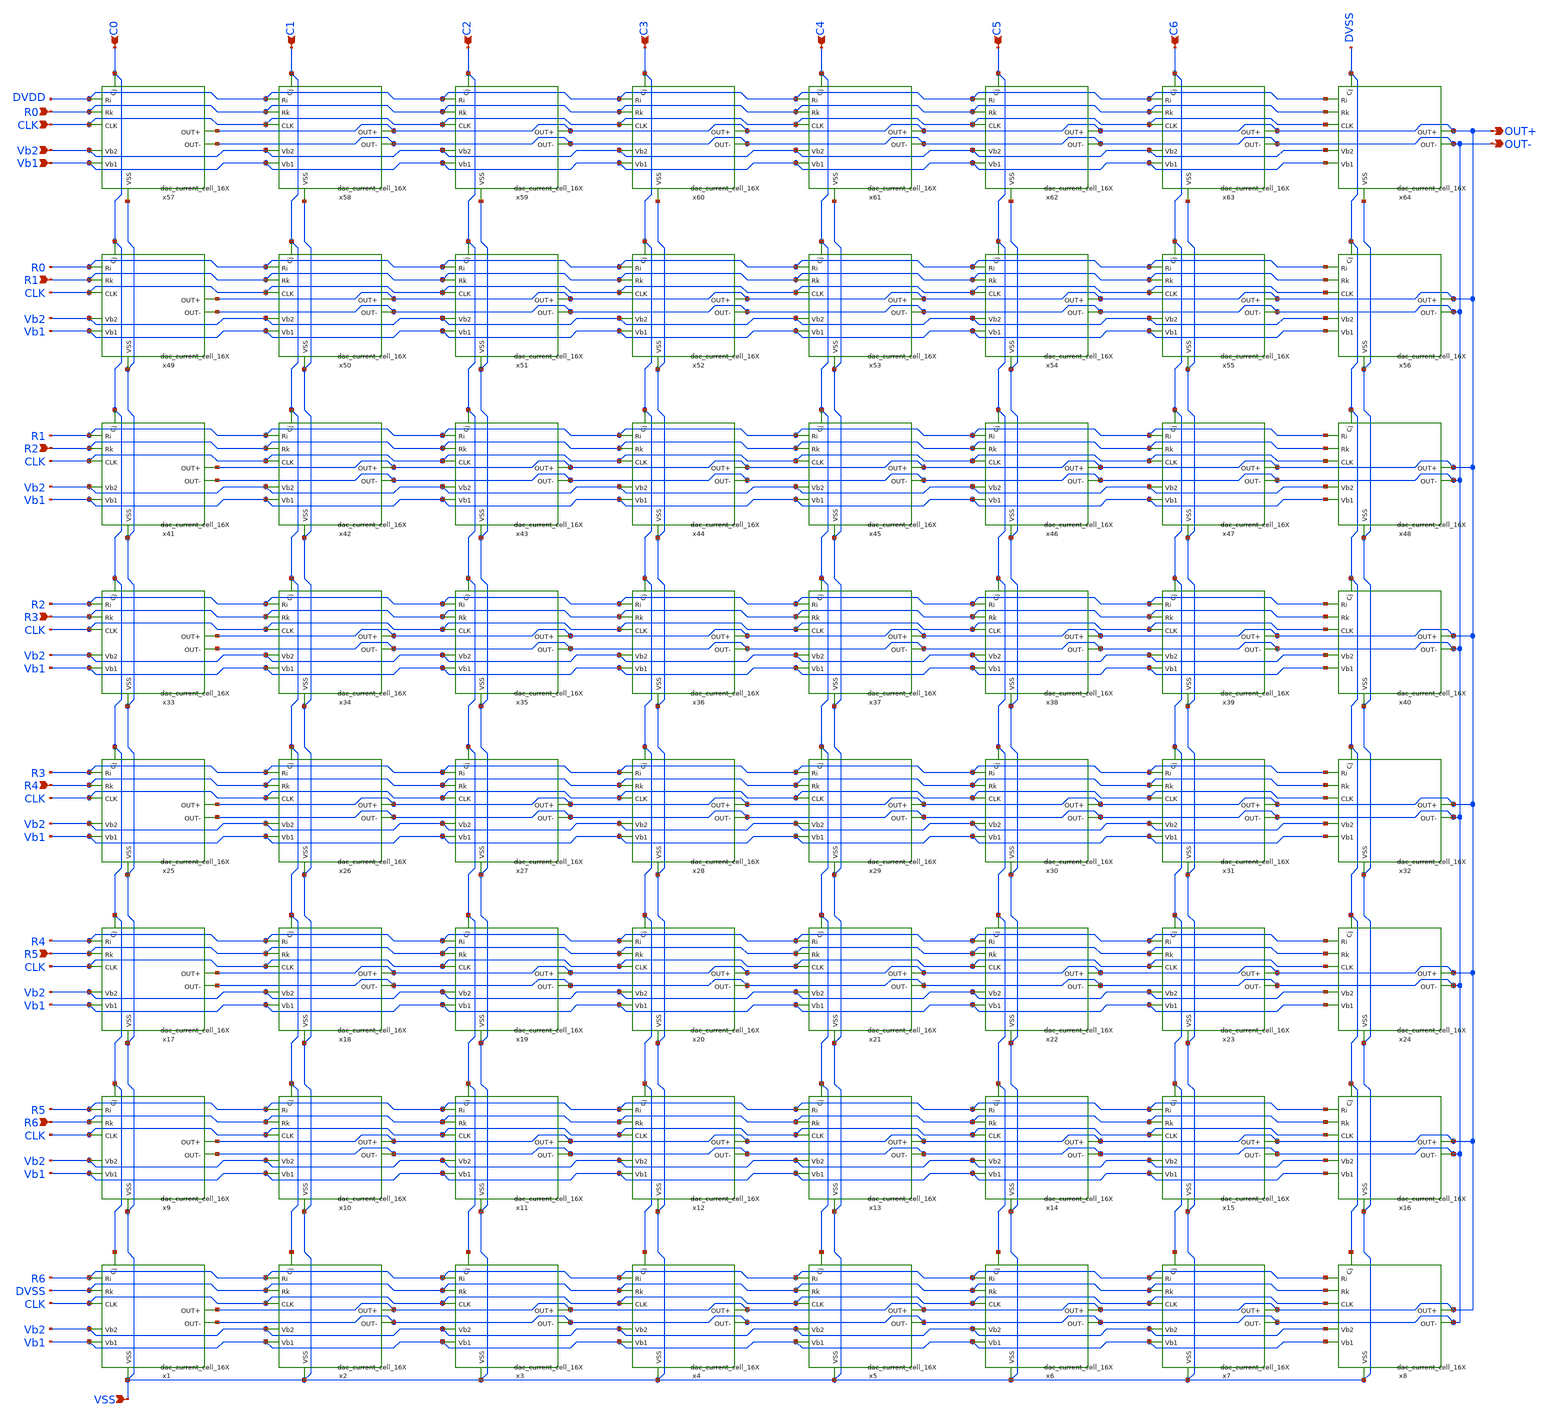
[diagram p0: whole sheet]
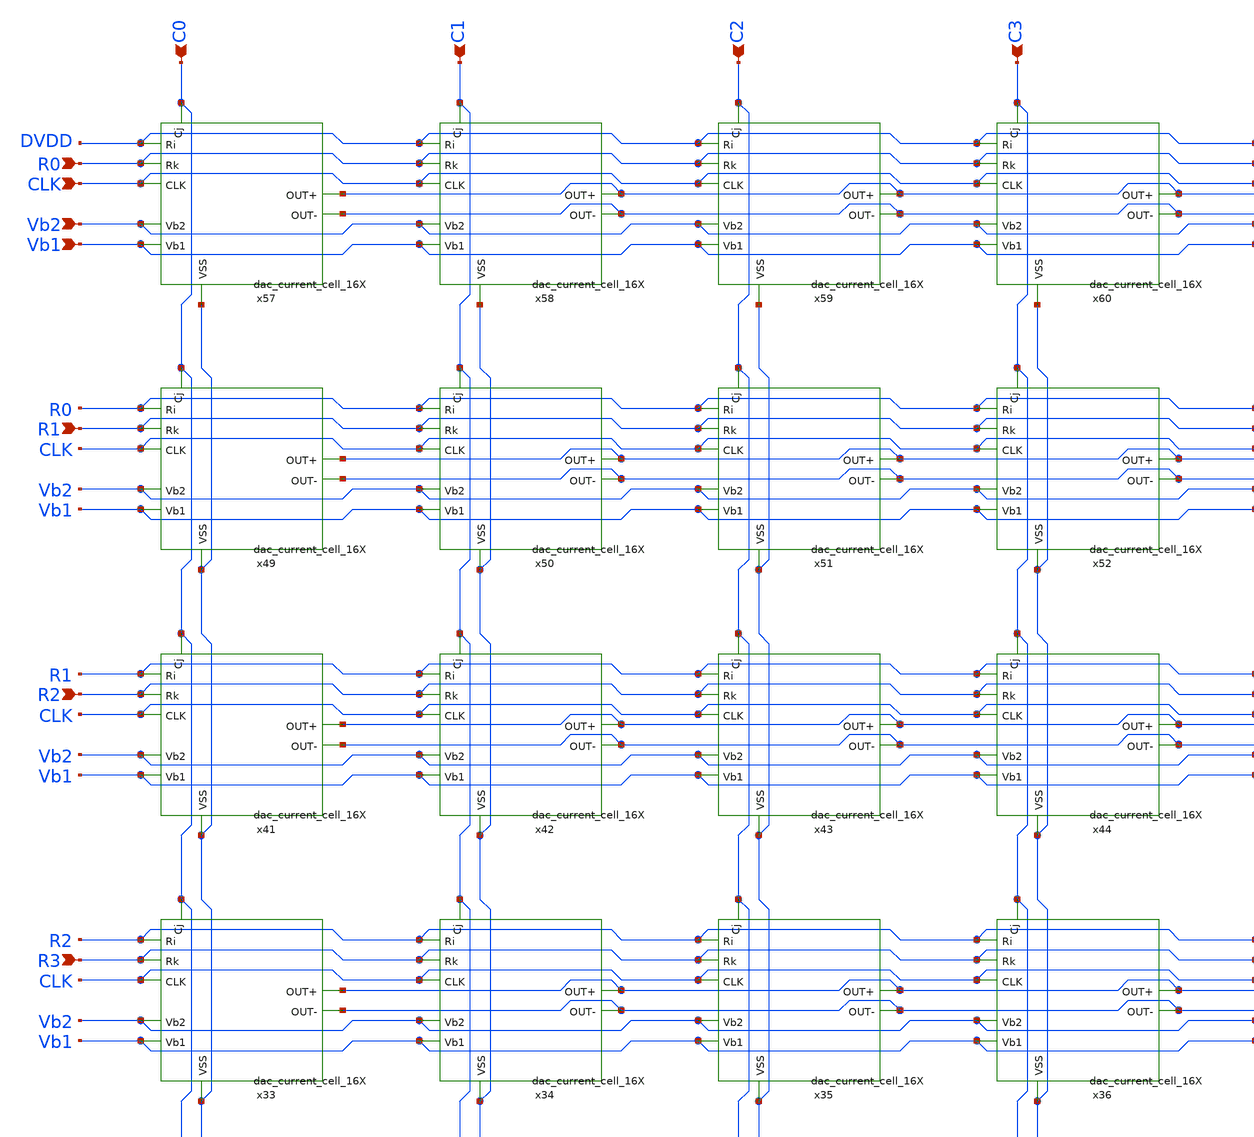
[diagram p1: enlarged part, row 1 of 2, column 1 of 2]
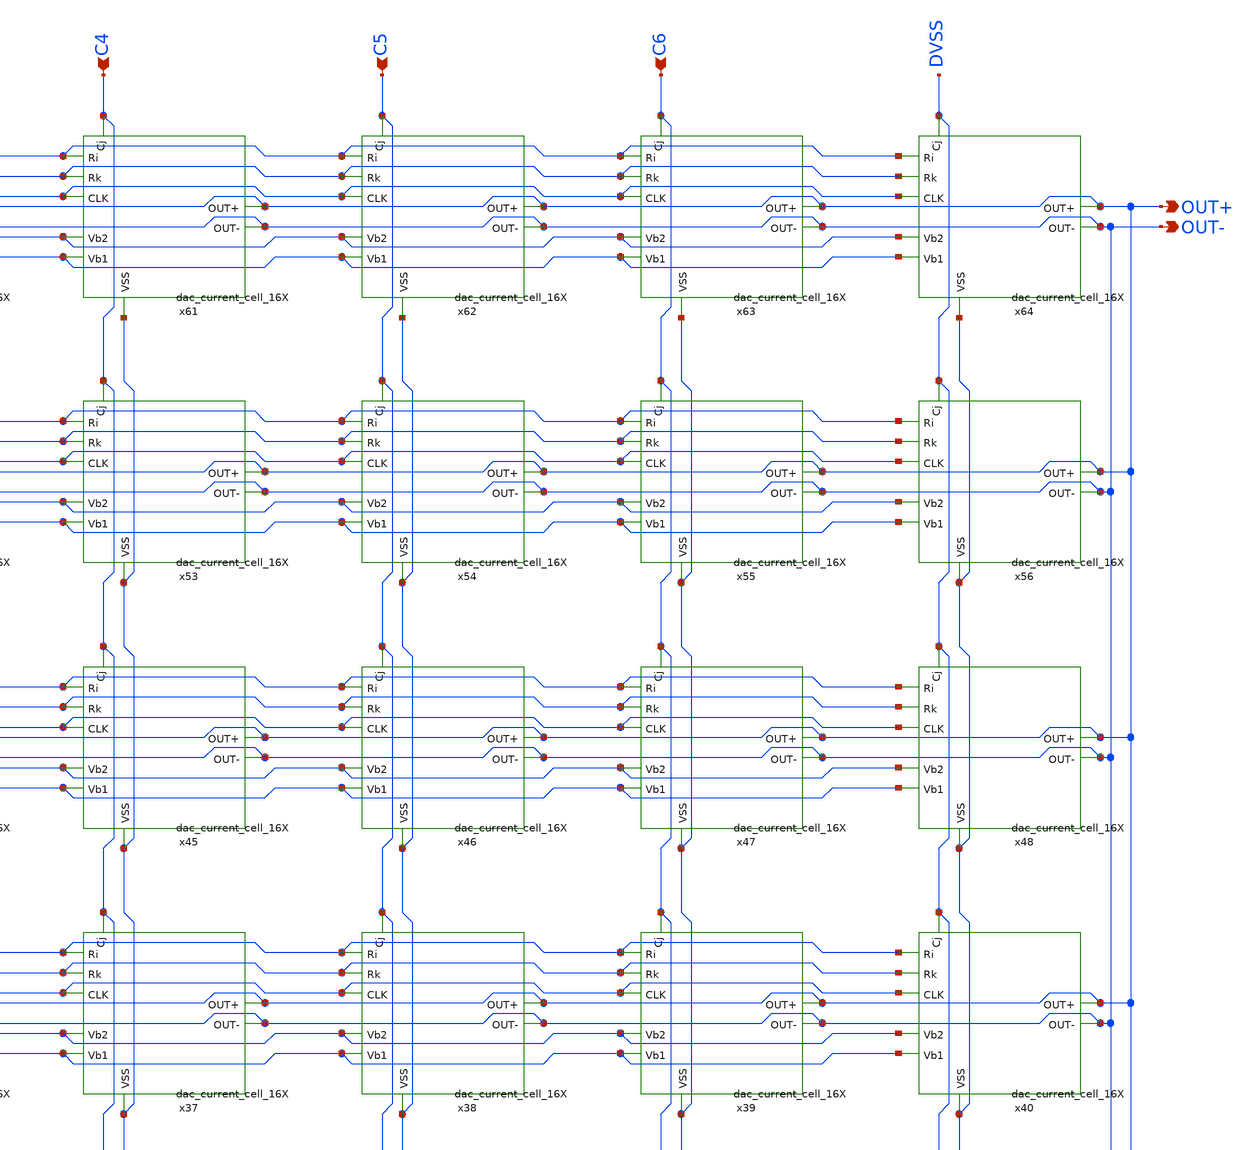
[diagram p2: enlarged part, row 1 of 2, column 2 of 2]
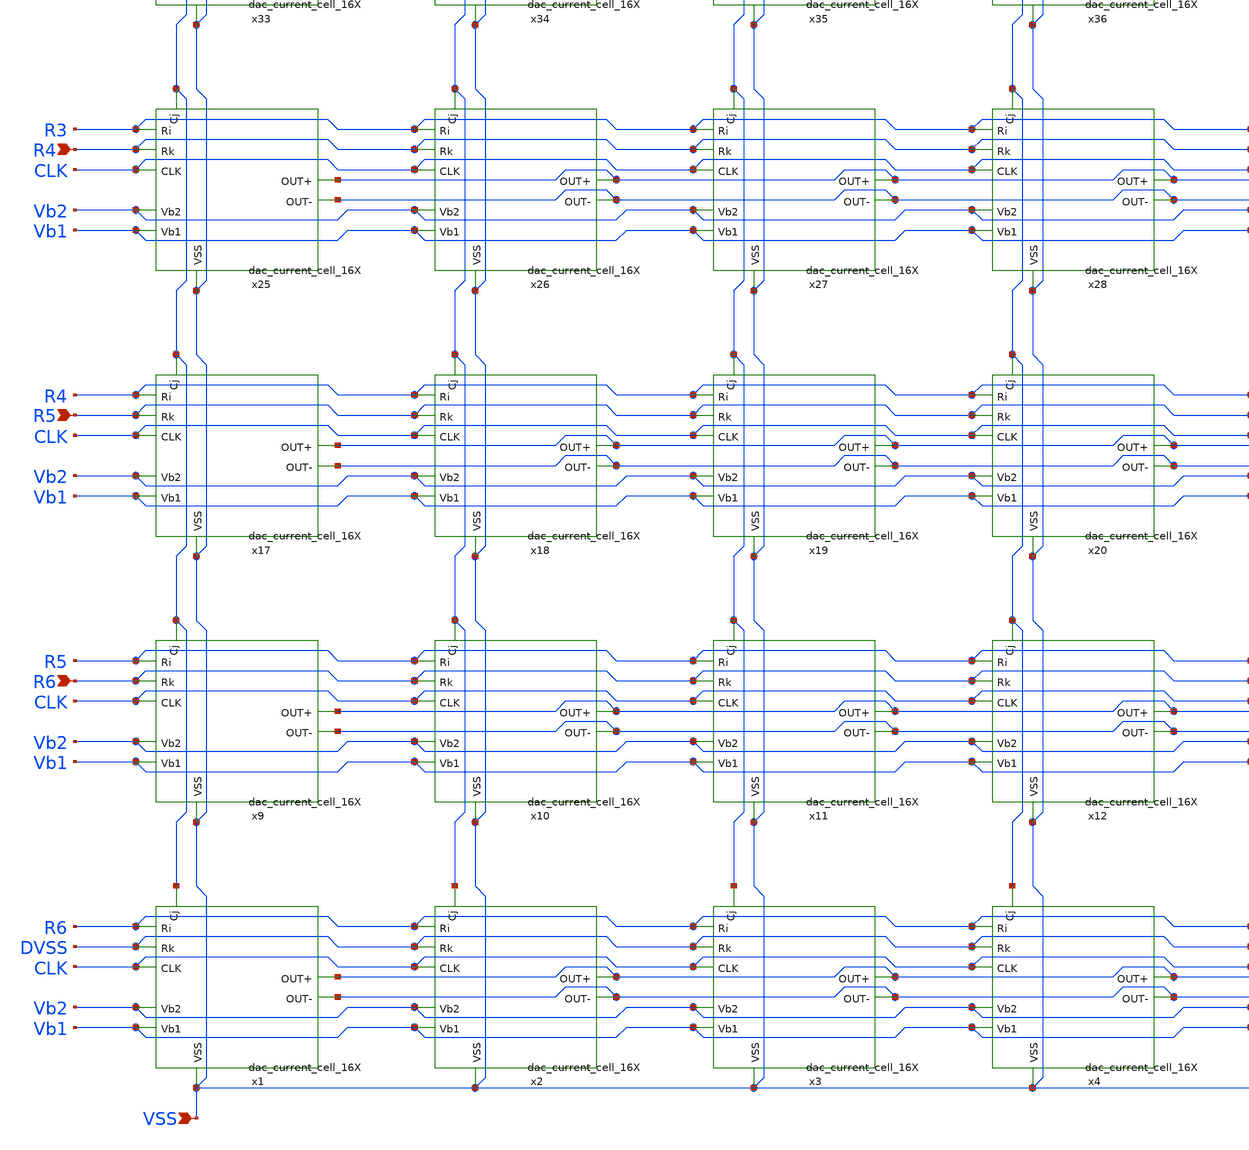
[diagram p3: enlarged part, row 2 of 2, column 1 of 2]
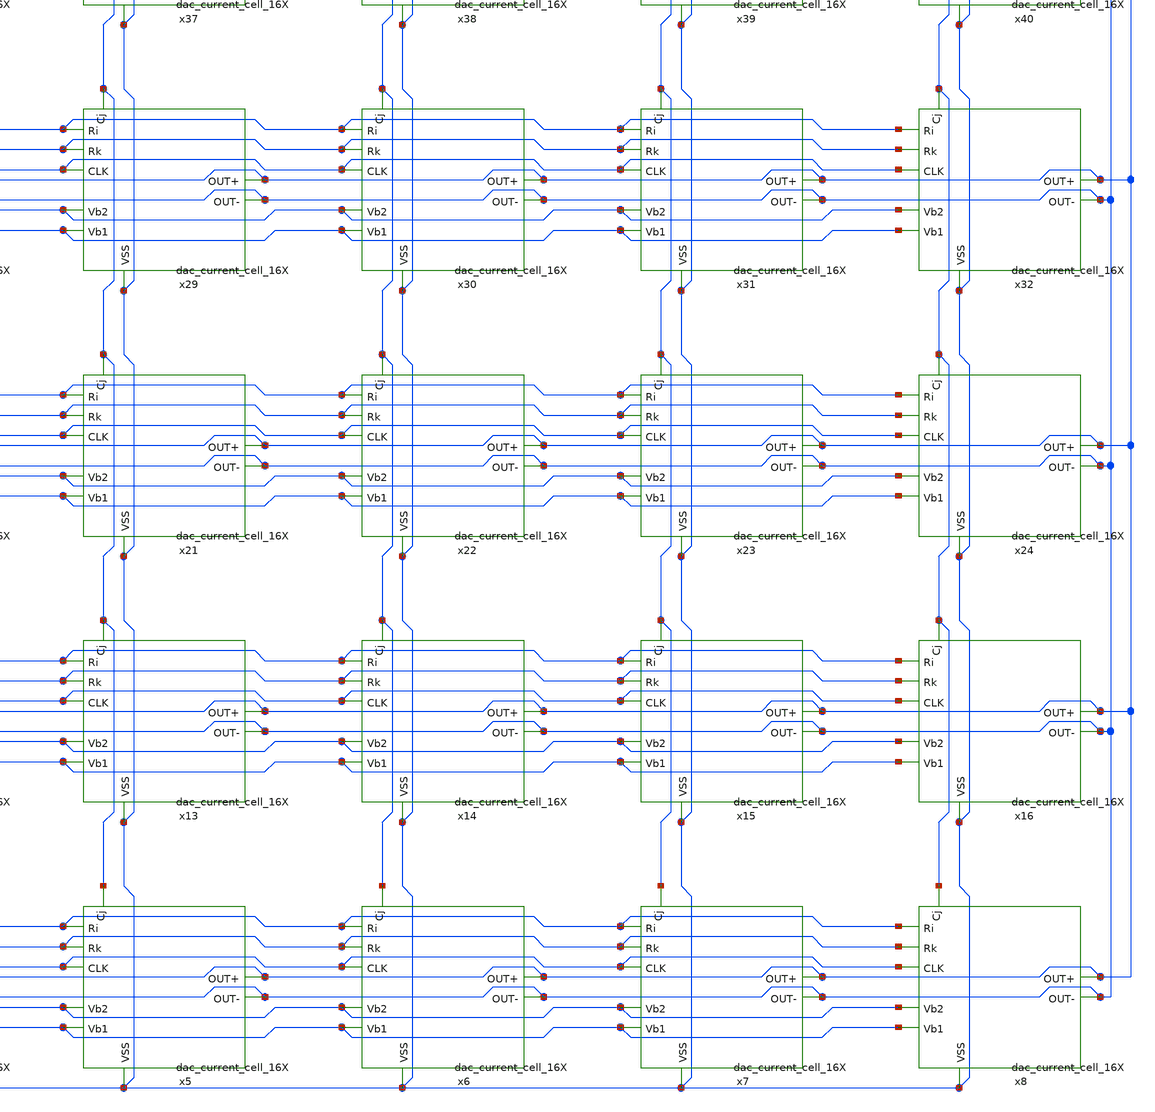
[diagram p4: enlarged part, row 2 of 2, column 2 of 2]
** sch_path: DAC/xschem/dac_msb_matrix.sch
**.subckt dac_msb_matrix R0 CLK R1 R2 R3 R4 R5 R6 C0 C1 C2 C3 C4 C5 C6 Vb2 Vb1 OUT+ OUT- VSS
*.ipin R0
*.ipin CLK
*.ipin R1
*.ipin R2
*.ipin R3
*.ipin R4
*.ipin R5
*.ipin R6
*.ipin C0
*.ipin C1
*.ipin C2
*.ipin C3
*.ipin C4
*.ipin C5
*.ipin C6
*.ipin Vb2
*.ipin Vb1
*.opin OUT+
*.opin OUT-
*.ipin VSS
x1 C0 R6 OUT+ OUT- CLK DVSS Vb2 Vb1 VSS DVDD DVNW DVPW DVSS dac_current_cell_16X
x2 C1 R6 OUT+ OUT- CLK DVSS Vb2 Vb1 VSS DVDD DVNW DVPW DVSS dac_current_cell_16X
x3 C2 R6 OUT+ OUT- CLK DVSS Vb2 Vb1 VSS DVDD DVNW DVPW DVSS dac_current_cell_16X
x4 C3 R6 OUT+ OUT- CLK DVSS Vb2 Vb1 VSS DVDD DVNW DVPW DVSS dac_current_cell_16X
x5 C4 R6 OUT+ OUT- CLK DVSS Vb2 Vb1 VSS DVDD DVNW DVPW DVSS dac_current_cell_16X
x6 C5 R6 OUT+ OUT- CLK DVSS Vb2 Vb1 VSS DVDD DVNW DVPW DVSS dac_current_cell_16X
x7 C6 R6 OUT+ OUT- CLK DVSS Vb2 Vb1 VSS DVDD DVNW DVPW DVSS dac_current_cell_16X
x8 DVSS R6 OUT+ OUT- CLK DVSS Vb2 Vb1 VSS DVDD DVNW DVPW DVSS dac_current_cell_16X
x9 C0 R5 OUT+ OUT- CLK R6 Vb2 Vb1 VSS DVDD DVNW DVPW DVSS dac_current_cell_16X
x10 C1 R5 OUT+ OUT- CLK R6 Vb2 Vb1 VSS DVDD DVNW DVPW DVSS dac_current_cell_16X
x11 C2 R5 OUT+ OUT- CLK R6 Vb2 Vb1 VSS DVDD DVNW DVPW DVSS dac_current_cell_16X
x12 C3 R5 OUT+ OUT- CLK R6 Vb2 Vb1 VSS DVDD DVNW DVPW DVSS dac_current_cell_16X
x13 C4 R5 OUT+ OUT- CLK R6 Vb2 Vb1 VSS DVDD DVNW DVPW DVSS dac_current_cell_16X
x14 C5 R5 OUT+ OUT- CLK R6 Vb2 Vb1 VSS DVDD DVNW DVPW DVSS dac_current_cell_16X
x15 C6 R5 OUT+ OUT- CLK R6 Vb2 Vb1 VSS DVDD DVNW DVPW DVSS dac_current_cell_16X
x16 DVSS R5 OUT+ OUT- CLK R6 Vb2 Vb1 VSS DVDD DVNW DVPW DVSS dac_current_cell_16X
x17 C0 R4 OUT+ OUT- CLK R5 Vb2 Vb1 VSS DVDD DVNW DVPW DVSS dac_current_cell_16X
x18 C1 R4 OUT+ OUT- CLK R5 Vb2 Vb1 VSS DVDD DVNW DVPW DVSS dac_current_cell_16X
x19 C2 R4 OUT+ OUT- CLK R5 Vb2 Vb1 VSS DVDD DVNW DVPW DVSS dac_current_cell_16X
x20 C3 R4 OUT+ OUT- CLK R5 Vb2 Vb1 VSS DVDD DVNW DVPW DVSS dac_current_cell_16X
x21 C4 R4 OUT+ OUT- CLK R5 Vb2 Vb1 VSS DVDD DVNW DVPW DVSS dac_current_cell_16X
x22 C5 R4 OUT+ OUT- CLK R5 Vb2 Vb1 VSS DVDD DVNW DVPW DVSS dac_current_cell_16X
x23 C6 R4 OUT+ OUT- CLK R5 Vb2 Vb1 VSS DVDD DVNW DVPW DVSS dac_current_cell_16X
x24 DVSS R4 OUT+ OUT- CLK R5 Vb2 Vb1 VSS DVDD DVNW DVPW DVSS dac_current_cell_16X
x25 C0 R3 OUT+ OUT- CLK R4 Vb2 Vb1 VSS DVDD DVNW DVPW DVSS dac_current_cell_16X
x26 C1 R3 OUT+ OUT- CLK R4 Vb2 Vb1 VSS DVDD DVNW DVPW DVSS dac_current_cell_16X
x27 C2 R3 OUT+ OUT- CLK R4 Vb2 Vb1 VSS DVDD DVNW DVPW DVSS dac_current_cell_16X
x28 C3 R3 OUT+ OUT- CLK R4 Vb2 Vb1 VSS DVDD DVNW DVPW DVSS dac_current_cell_16X
x29 C4 R3 OUT+ OUT- CLK R4 Vb2 Vb1 VSS DVDD DVNW DVPW DVSS dac_current_cell_16X
x30 C5 R3 OUT+ OUT- CLK R4 Vb2 Vb1 VSS DVDD DVNW DVPW DVSS dac_current_cell_16X
x31 C6 R3 OUT+ OUT- CLK R4 Vb2 Vb1 VSS DVDD DVNW DVPW DVSS dac_current_cell_16X
x32 DVSS R3 OUT+ OUT- CLK R4 Vb2 Vb1 VSS DVDD DVNW DVPW DVSS dac_current_cell_16X
x33 C0 R2 OUT+ OUT- CLK R3 Vb2 Vb1 VSS DVDD DVNW DVPW DVSS dac_current_cell_16X
x34 C1 R2 OUT+ OUT- CLK R3 Vb2 Vb1 VSS DVDD DVNW DVPW DVSS dac_current_cell_16X
x35 C2 R2 OUT+ OUT- CLK R3 Vb2 Vb1 VSS DVDD DVNW DVPW DVSS dac_current_cell_16X
x36 C3 R2 OUT+ OUT- CLK R3 Vb2 Vb1 VSS DVDD DVNW DVPW DVSS dac_current_cell_16X
x37 C4 R2 OUT+ OUT- CLK R3 Vb2 Vb1 VSS DVDD DVNW DVPW DVSS dac_current_cell_16X
x38 C5 R2 OUT+ OUT- CLK R3 Vb2 Vb1 VSS DVDD DVNW DVPW DVSS dac_current_cell_16X
x39 C6 R2 OUT+ OUT- CLK R3 Vb2 Vb1 VSS DVDD DVNW DVPW DVSS dac_current_cell_16X
x40 DVSS R2 OUT+ OUT- CLK R3 Vb2 Vb1 VSS DVDD DVNW DVPW DVSS dac_current_cell_16X
x41 C0 R1 OUT+ OUT- CLK R2 Vb2 Vb1 VSS DVDD DVNW DVPW DVSS dac_current_cell_16X
x42 C1 R1 OUT+ OUT- CLK R2 Vb2 Vb1 VSS DVDD DVNW DVPW DVSS dac_current_cell_16X
x43 C2 R1 OUT+ OUT- CLK R2 Vb2 Vb1 VSS DVDD DVNW DVPW DVSS dac_current_cell_16X
x44 C3 R1 OUT+ OUT- CLK R2 Vb2 Vb1 VSS DVDD DVNW DVPW DVSS dac_current_cell_16X
x45 C4 R1 OUT+ OUT- CLK R2 Vb2 Vb1 VSS DVDD DVNW DVPW DVSS dac_current_cell_16X
x46 C5 R1 OUT+ OUT- CLK R2 Vb2 Vb1 VSS DVDD DVNW DVPW DVSS dac_current_cell_16X
x47 C6 R1 OUT+ OUT- CLK R2 Vb2 Vb1 VSS DVDD DVNW DVPW DVSS dac_current_cell_16X
x48 DVSS R1 OUT+ OUT- CLK R2 Vb2 Vb1 VSS DVDD DVNW DVPW DVSS dac_current_cell_16X
x49 C0 R0 OUT+ OUT- CLK R1 Vb2 Vb1 VSS DVDD DVNW DVPW DVSS dac_current_cell_16X
x50 C1 R0 OUT+ OUT- CLK R1 Vb2 Vb1 VSS DVDD DVNW DVPW DVSS dac_current_cell_16X
x51 C2 R0 OUT+ OUT- CLK R1 Vb2 Vb1 VSS DVDD DVNW DVPW DVSS dac_current_cell_16X
x52 C3 R0 OUT+ OUT- CLK R1 Vb2 Vb1 VSS DVDD DVNW DVPW DVSS dac_current_cell_16X
x53 C4 R0 OUT+ OUT- CLK R1 Vb2 Vb1 VSS DVDD DVNW DVPW DVSS dac_current_cell_16X
x54 C5 R0 OUT+ OUT- CLK R1 Vb2 Vb1 VSS DVDD DVNW DVPW DVSS dac_current_cell_16X
x55 C6 R0 OUT+ OUT- CLK R1 Vb2 Vb1 VSS DVDD DVNW DVPW DVSS dac_current_cell_16X
x56 DVSS R0 OUT+ OUT- CLK R1 Vb2 Vb1 VSS DVDD DVNW DVPW DVSS dac_current_cell_16X
x57 C0 DVDD OUT+ OUT- CLK R0 Vb2 Vb1 VSS DVDD DVNW DVPW DVSS dac_current_cell_16X
x58 C1 DVDD OUT+ OUT- CLK R0 Vb2 Vb1 VSS DVDD DVNW DVPW DVSS dac_current_cell_16X
x59 C2 DVDD OUT+ OUT- CLK R0 Vb2 Vb1 VSS DVDD DVNW DVPW DVSS dac_current_cell_16X
x60 C3 DVDD OUT+ OUT- CLK R0 Vb2 Vb1 VSS DVDD DVNW DVPW DVSS dac_current_cell_16X
x61 C4 DVDD OUT+ OUT- CLK R0 Vb2 Vb1 VSS DVDD DVNW DVPW DVSS dac_current_cell_16X
x62 C5 DVDD OUT+ OUT- CLK R0 Vb2 Vb1 VSS DVDD DVNW DVPW DVSS dac_current_cell_16X
x63 C6 DVDD OUT+ OUT- CLK R0 Vb2 Vb1 VSS DVDD DVNW DVPW DVSS dac_current_cell_16X
x64 DVSS DVDD OUT+ OUT- CLK R0 Vb2 Vb1 VSS DVDD DVNW DVPW DVSS dac_current_cell_16X
**.ends
.end
